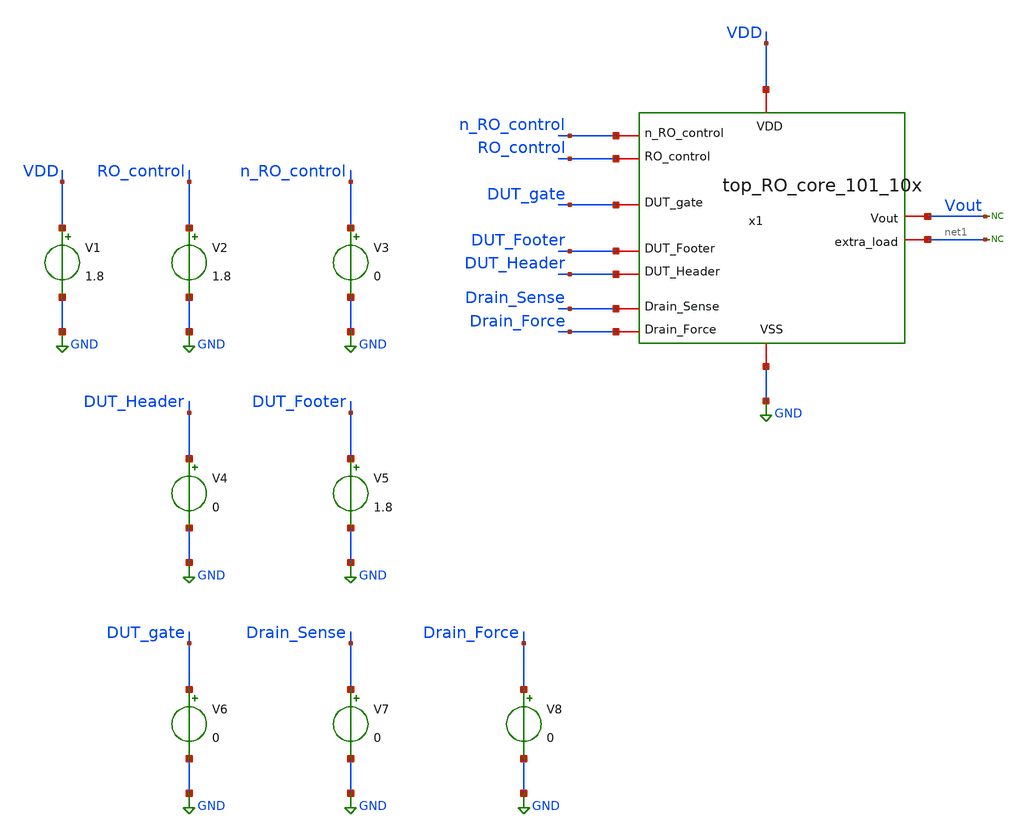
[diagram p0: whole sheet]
** sch_path: TT/top_RO_core_101_10x_tb.sch
.lib $::SKYWATER_MODELS/sky130.lib.spice tt
.include $::SKYWATER_STDCELLS/sky130_fd_sc_hd.spice

**.subckt top_RO_core_101_10x_tb
V1 VDD GND 1.8
V2 RO_control GND 1.8
V3 n_RO_control GND 0
V4 DUT_Header GND 0
V5 DUT_Footer GND 1.8
* noconn #net1
* noconn Vout
V6 DUT_gate GND 0
V7 Drain_Sense GND 0
V8 Drain_Force GND 0
x1 VDD GND n_RO_control RO_control DUT_gate Vout DUT_Header DUT_Footer Drain_Force Drain_Sense net1
+ top_RO_core_101_10x
**** begin user architecture code


.ic V(x1.A[8])=0.8
.tran 0.1n 50n
.save all



**** end user architecture code
**.ends

* expanding   symbol:  /foss/designs/Projects/RO_reliability/xschem/top_RO_core_101_10x.sym # of
*+ pins=11
** sym_path: TT/top_RO_core_101_10x.sym
** sch_path: TT/top_RO_core_101_10x.sch
.subckt top_RO_core_101_10x VDD VSS n_RO_control RO_control DUT_gate Vout DUT_Header DUT_Footer
+ Drain_Force Drain_Sense extra_load
*.iopin VDD
*.iopin VSS
*.iopin n_RO_control
*.iopin RO_control
*.iopin DUT_gate
*.iopin extra_load
*.iopin DUT_Header
*.iopin DUT_Footer
*.iopin Drain_Force
*.iopin Drain_Sense
*.iopin Vout
x1[1] VDD VSS A[96] A[95] rovcel2
x1[2] VDD VSS A[95] A[94] rovcel2
x1[3] VDD VSS A[94] A[93] rovcel2
x1[4] VDD VSS A[93] A[92] rovcel2
x1[5] VDD VSS A[92] A[91] rovcel2
x1[6] VDD VSS A[91] A[90] rovcel2
x1[7] VDD VSS A[90] A[89] rovcel2
x1[8] VDD VSS A[89] A[88] rovcel2
x1[9] VDD VSS A[88] A[87] rovcel2
x1[10] VDD VSS A[87] A[86] rovcel2
x1[11] VDD VSS A[86] A[85] rovcel2
x1[12] VDD VSS A[85] A[84] rovcel2
x1[13] VDD VSS A[84] A[83] rovcel2
x1[14] VDD VSS A[83] A[82] rovcel2
x1[15] VDD VSS A[82] A[81] rovcel2
x1[16] VDD VSS A[81] A[80] rovcel2
x1[17] VDD VSS A[80] A[79] rovcel2
x1[18] VDD VSS A[79] A[78] rovcel2
x1[19] VDD VSS A[78] A[77] rovcel2
x1[20] VDD VSS A[77] A[76] rovcel2
x1[21] VDD VSS A[76] A[75] rovcel2
x1[22] VDD VSS A[75] A[74] rovcel2
x1[23] VDD VSS A[74] A[73] rovcel2
x1[24] VDD VSS A[73] A[72] rovcel2
x1[25] VDD VSS A[72] A[71] rovcel2
x1[26] VDD VSS A[71] A[70] rovcel2
x1[27] VDD VSS A[70] A[69] rovcel2
x1[28] VDD VSS A[69] A[68] rovcel2
x1[29] VDD VSS A[68] A[67] rovcel2
x1[30] VDD VSS A[67] A[66] rovcel2
x1[31] VDD VSS A[66] A[65] rovcel2
x1[32] VDD VSS A[65] A[64] rovcel2
x1[33] VDD VSS A[64] A[63] rovcel2
x1[34] VDD VSS A[63] A[62] rovcel2
x1[35] VDD VSS A[62] A[61] rovcel2
x1[36] VDD VSS A[61] A[60] rovcel2
x1[37] VDD VSS A[60] A[59] rovcel2
x1[38] VDD VSS A[59] A[58] rovcel2
x1[39] VDD VSS A[58] A[57] rovcel2
x1[40] VDD VSS A[57] A[56] rovcel2
x1[41] VDD VSS A[56] A[55] rovcel2
x1[42] VDD VSS A[55] A[54] rovcel2
x1[43] VDD VSS A[54] A[53] rovcel2
x1[44] VDD VSS A[53] A[52] rovcel2
x1[45] VDD VSS A[52] A[51] rovcel2
x1[46] VDD VSS A[51] A[50] rovcel2
x1[47] VDD VSS A[50] A[49] rovcel2
x1[48] VDD VSS A[49] A[48] rovcel2
x1[49] VDD VSS A[48] A[47] rovcel2
x1[50] VDD VSS A[47] A[46] rovcel2
x1[51] VDD VSS A[46] A[45] rovcel2
x1[52] VDD VSS A[45] A[44] rovcel2
x1[53] VDD VSS A[44] A[43] rovcel2
x1[54] VDD VSS A[43] A[42] rovcel2
x1[55] VDD VSS A[42] A[41] rovcel2
x1[56] VDD VSS A[41] A[40] rovcel2
x1[57] VDD VSS A[40] A[39] rovcel2
x1[58] VDD VSS A[39] A[38] rovcel2
x1[59] VDD VSS A[38] A[37] rovcel2
x1[60] VDD VSS A[37] A[36] rovcel2
x1[61] VDD VSS A[36] A[35] rovcel2
x1[62] VDD VSS A[35] A[34] rovcel2
x1[63] VDD VSS A[34] A[33] rovcel2
x1[64] VDD VSS A[33] A[32] rovcel2
x1[65] VDD VSS A[32] A[31] rovcel2
x1[66] VDD VSS A[31] A[30] rovcel2
x1[67] VDD VSS A[30] A[29] rovcel2
x1[68] VDD VSS A[29] A[28] rovcel2
x1[69] VDD VSS A[28] A[27] rovcel2
x1[70] VDD VSS A[27] A[26] rovcel2
x1[71] VDD VSS A[26] A[25] rovcel2
x1[72] VDD VSS A[25] A[24] rovcel2
x1[73] VDD VSS A[24] A[23] rovcel2
x1[74] VDD VSS A[23] A[22] rovcel2
x1[75] VDD VSS A[22] A[21] rovcel2
x1[76] VDD VSS A[21] A[20] rovcel2
x1[77] VDD VSS A[20] A[19] rovcel2
x1[78] VDD VSS A[19] A[18] rovcel2
x1[79] VDD VSS A[18] A[17] rovcel2
x1[80] VDD VSS A[17] A[16] rovcel2
x1[81] VDD VSS A[16] A[15] rovcel2
x1[82] VDD VSS A[15] A[14] rovcel2
x1[83] VDD VSS A[14] A[13] rovcel2
x1[84] VDD VSS A[13] A[12] rovcel2
x1[85] VDD VSS A[12] A[11] rovcel2
x1[86] VDD VSS A[11] A[10] rovcel2
x1[87] VDD VSS A[10] A[9] rovcel2
x1[88] VDD VSS A[9] A[8] rovcel2
x1[89] VDD VSS A[8] A[7] rovcel2
x1[90] VDD VSS A[7] A[6] rovcel2
x1[91] VDD VSS A[6] A[5] rovcel2
x1[92] VDD VSS A[5] A[4] rovcel2
x1[93] VDD VSS A[4] A[3] rovcel2
x1[94] VDD VSS A[3] A[2] rovcel2
x1[95] VDD VSS A[2] A[1] rovcel2
x1[96] VDD VSS A[1] Vout rovcel2
x2 VDD VSS A[97] n_RO_control A[98] RO_control DUT_gate rovcel3
x3 VDD VSS A[97] A[96] rovcel2
x5 VDD VSS extra_load n_RO_control A[100] rovcel4
x6 VDD VSS Vout A[100] rovcel2
x1 DUT_Header DUT_Footer Drain_Force Drain_Sense RO_control n_RO_control VDD VSS A[98] extra_load
+ rovcel1_10
.ends


* expanding   symbol:  /foss/designs/Projects/RO_reliability/xschem/rovcel2.sym # of pins=4
** sym_path: TT/rovcel2.sym
** sch_path: TT/rovcel2.sch
.subckt rovcel2 VDD VSS Vout Vin
*.iopin VDD
*.iopin VSS
*.iopin Vin
*.iopin Vout
x1 VDD Vin Vout VSS inverter_RO_rel
x2 VDD VDD Vout net1 VSS VSS tgate
x3 VDD VDD Vout net2 VSS VSS tgate
* noconn #net1
* noconn #net2
.ends


* expanding   symbol:  /foss/designs/Projects/RO_reliability/xschem/rovcel3.sym # of pins=7
** sym_path: TT/rovcel3.sym
** sch_path: TT/rovcel3.sch
.subckt rovcel3 VDD VSS Vin n_RO_control Vout RO_control DUT_gate
*.iopin VDD
*.iopin VSS
*.iopin Vin
*.iopin n_RO_control
*.iopin RO_control
*.iopin DUT_gate
*.iopin Vout
* noconn #net1
x4 VDD VSS Vin n_RO_control RO_control Vout tristate_inv
x1 RO_control VDD Vout net1 VSS n_RO_control tgate
x5 RO_control VDD Vout DUT_gate VSS n_RO_control tgate
.ends


* expanding   symbol:  /foss/designs/Projects/RO_reliability/xschem/rovcel4.sym # of pins=5
** sym_path: TT/rovcel4.sym
** sch_path: TT/rovcel4.sch
.subckt rovcel4 VDD VSS Vin n_RO_control Vout
*.iopin VDD
*.iopin VSS
*.iopin Vin
*.iopin n_RO_control
*.iopin Vout
* noconn #net1
x4 n_RO_control VDD VSS Vin Vout inv1
x1 VDD VDD Vout VSS VSS VSS tgate
x5 VDD VDD Vout net1 VSS VSS tgate
.ends


* expanding   symbol:  /foss/designs/Projects/RO_reliability/xschem/rovcel1_10.sym # of pins=10
** sym_path: TT/rovcel1_10.sym
** sch_path: TT/rovcel1_10.sch
.subckt rovcel1_10 DUT_Header DUT_Footer Drain_Force Drain_Sense RO_control n_RO_control VDD VSS Vin
+ Vout
*.iopin VDD
*.iopin VSS
*.iopin Vin
*.iopin DUT_Header
*.iopin DUT_Footer
*.iopin Drain_Force
*.iopin Vout
*.iopin Drain_Sense
*.iopin RO_control
*.iopin n_RO_control
x1 VDD VSS Vin DUT_Header DUT_Footer Vout tristate_inv
x2 RO_control VDD Vout Drain_Sense VSS n_RO_control tgate
x3 RO_control VDD Vout Drain_Force VSS n_RO_control tgate_force10
.ends


* expanding   symbol:  /foss/designs/Projects/RO_reliability/xschem/inverter_RO_rel.sym # of pins=4
** sym_path: TT/inverter_RO_rel.sym
** sch_path: TT/inverter_RO_rel.sch
.subckt inverter_RO_rel VDD Vin Vout VSS
*.iopin VDD
*.iopin VSS
*.iopin Vin
*.iopin Vout
XM2 Vout Vin VDD VDD sky130_fd_pr__pfet_01v8 L=0.15 W=4.75 nf=1 ad='int((nf+1)/2) * W/nf * 0.29' as='int((nf+2)/2) * W/nf * 0.29'
+ pd='2*int((nf+1)/2) * (W/nf + 0.29)' ps='2*int((nf+2)/2) * (W/nf + 0.29)' nrd='0.29 / W' nrs='0.29 / W'
+ sa=0 sb=0 sd=0 mult=4 m=4
XM1 Vout Vin VSS VSS sky130_fd_pr__nfet_01v8 L=0.15 W=2.1 nf=1 ad='int((nf+1)/2) * W/nf * 0.29' as='int((nf+2)/2) * W/nf * 0.29'
+ pd='2*int((nf+1)/2) * (W/nf + 0.29)' ps='2*int((nf+2)/2) * (W/nf + 0.29)' nrd='0.29 / W' nrs='0.29 / W'
+ sa=0 sb=0 sd=0 mult=2 m=2
.ends


* expanding   symbol:  /foss/designs/Projects/RO_reliability/xschem/tgate.sym # of pins=6
** sym_path: TT/tgate.sym
** sch_path: TT/tgate.sch
.subckt tgate nclk VDD Vin Vout VSS clk
*.iopin nclk
*.iopin clk
*.iopin VDD
*.iopin VSS
*.iopin Vout
*.iopin Vin
XM1 Vin nclk Vout VDD sky130_fd_pr__pfet_01v8 L=0.15 W=0.45 nf=1 ad='int((nf+1)/2) * W/nf * 0.29' as='int((nf+2)/2) * W/nf * 0.29'
+ pd='2*int((nf+1)/2) * (W/nf + 0.29)' ps='2*int((nf+2)/2) * (W/nf + 0.29)' nrd='0.29 / W' nrs='0.29 / W'
+ sa=0 sb=0 sd=0 mult=1 m=1
XM2 Vin clk Vout VSS sky130_fd_pr__nfet_01v8 L=0.15 W=0.45 nf=1 ad='int((nf+1)/2) * W/nf * 0.29' as='int((nf+2)/2) * W/nf * 0.29'
+ pd='2*int((nf+1)/2) * (W/nf + 0.29)' ps='2*int((nf+2)/2) * (W/nf + 0.29)' nrd='0.29 / W' nrs='0.29 / W'
+ sa=0 sb=0 sd=0 mult=1 m=1
.ends


* expanding   symbol:  /foss/designs/RO_Aging_UNICASS/TT/tristate_inv.sym # of pins=6
** sym_path: TT/tristate_inv.sym
** sch_path: TT/tristate_inv.sch
.subckt tristate_inv VDD VSS Vin Vup Vdn Vout
*.iopin VDD
*.iopin VSS
*.iopin Vin
*.iopin Vout
*.iopin Vup
*.iopin Vdn
XM1 net1 Vup VDD VDD sky130_fd_pr__pfet_01v8 L=0.15 W=4.75 nf=1 ad='int((nf+1)/2) * W/nf * 0.29' as='int((nf+2)/2) * W/nf * 0.29'
+ pd='2*int((nf+1)/2) * (W/nf + 0.29)' ps='2*int((nf+2)/2) * (W/nf + 0.29)' nrd='0.29 / W' nrs='0.29 / W'
+ sa=0 sb=0 sd=0 mult=40 m=40
XM2 Vout Vin net1 VDD sky130_fd_pr__pfet_01v8 L=0.15 W=4.75 nf=1 ad='int((nf+1)/2) * W/nf * 0.29' as='int((nf+2)/2) * W/nf * 0.29'
+ pd='2*int((nf+1)/2) * (W/nf + 0.29)' ps='2*int((nf+2)/2) * (W/nf + 0.29)' nrd='0.29 / W' nrs='0.29 / W'
+ sa=0 sb=0 sd=0 mult=4 m=4
XM3 Vout Vin net2 VSS sky130_fd_pr__nfet_01v8 L=0.15 W=2.1 nf=1 ad='int((nf+1)/2) * W/nf * 0.29' as='int((nf+2)/2) * W/nf * 0.29'
+ pd='2*int((nf+1)/2) * (W/nf + 0.29)' ps='2*int((nf+2)/2) * (W/nf + 0.29)' nrd='0.29 / W' nrs='0.29 / W'
+ sa=0 sb=0 sd=0 mult=2 m=2
XM4 net2 Vdn VSS VSS sky130_fd_pr__nfet_01v8 L=0.15 W=2.1 nf=1 ad='int((nf+1)/2) * W/nf * 0.29' as='int((nf+2)/2) * W/nf * 0.29'
+ pd='2*int((nf+1)/2) * (W/nf + 0.29)' ps='2*int((nf+2)/2) * (W/nf + 0.29)' nrd='0.29 / W' nrs='0.29 / W'
+ sa=0 sb=0 sd=0 mult=20 m=20
.ends


* expanding   symbol:  /foss/designs/RO_Aging_UNICASS/TT/inv1.sym # of pins=5
** sym_path: TT/inv1.sym
** sch_path: TT/inv1.sch
.subckt inv1 n_RO_control VDD VSS Vin Vout
*.iopin VDD
*.iopin VSS
*.iopin Vin
*.iopin Vout
*.iopin n_RO_control
XM1 net1 n_RO_control VDD VDD sky130_fd_pr__pfet_01v8 L=0.15 W=4.75 nf=1 ad='int((nf+1)/2) * W/nf * 0.29'
+ as='int((nf+2)/2) * W/nf * 0.29' pd='2*int((nf+1)/2) * (W/nf + 0.29)' ps='2*int((nf+2)/2) * (W/nf + 0.29)'
+ nrd='0.29 / W' nrs='0.29 / W' sa=0 sb=0 sd=0 mult=40 m=40
XM2 Vout Vin net1 VDD sky130_fd_pr__pfet_01v8 L=0.15 W=4.75 nf=1 ad='int((nf+1)/2) * W/nf * 0.29' as='int((nf+2)/2) * W/nf * 0.29'
+ pd='2*int((nf+1)/2) * (W/nf + 0.29)' ps='2*int((nf+2)/2) * (W/nf + 0.29)' nrd='0.29 / W' nrs='0.29 / W'
+ sa=0 sb=0 sd=0 mult=4 m=4
XM3 Vout Vin VSS VSS sky130_fd_pr__nfet_01v8 L=0.15 W=2.1 nf=1 ad='int((nf+1)/2) * W/nf * 0.29' as='int((nf+2)/2) * W/nf * 0.29'
+ pd='2*int((nf+1)/2) * (W/nf + 0.29)' ps='2*int((nf+2)/2) * (W/nf + 0.29)' nrd='0.29 / W' nrs='0.29 / W'
+ sa=0 sb=0 sd=0 mult=2 m=2
.ends


* expanding   symbol:  /foss/designs/Projects/RO_reliability/xschem/tgate_force10.sym # of pins=6
** sym_path: TT/tgate_force10.sym
** sch_path: TT/tgate_force10.sch
.subckt tgate_force10 nclk VDD Vin Vout VSS clk
*.iopin nclk
*.iopin clk
*.iopin VDD
*.iopin VSS
*.iopin Vout
*.iopin Vin
XM1 Vin nclk Vout VDD sky130_fd_pr__pfet_01v8 L=0.15 W=4.75 nf=1 ad='int((nf+1)/2) * W/nf * 0.29' as='int((nf+2)/2) * W/nf * 0.29'
+ pd='2*int((nf+1)/2) * (W/nf + 0.29)' ps='2*int((nf+2)/2) * (W/nf + 0.29)' nrd='0.29 / W' nrs='0.29 / W'
+ sa=0 sb=0 sd=0 mult=40 m=40
XM2 Vin clk Vout VSS sky130_fd_pr__nfet_01v8 L=0.15 W=2.1 nf=1 ad='int((nf+1)/2) * W/nf * 0.29' as='int((nf+2)/2) * W/nf * 0.29'
+ pd='2*int((nf+1)/2) * (W/nf + 0.29)' ps='2*int((nf+2)/2) * (W/nf + 0.29)' nrd='0.29 / W' nrs='0.29 / W'
+ sa=0 sb=0 sd=0 mult=20 m=20
.ends

.GLOBAL GND
.end
